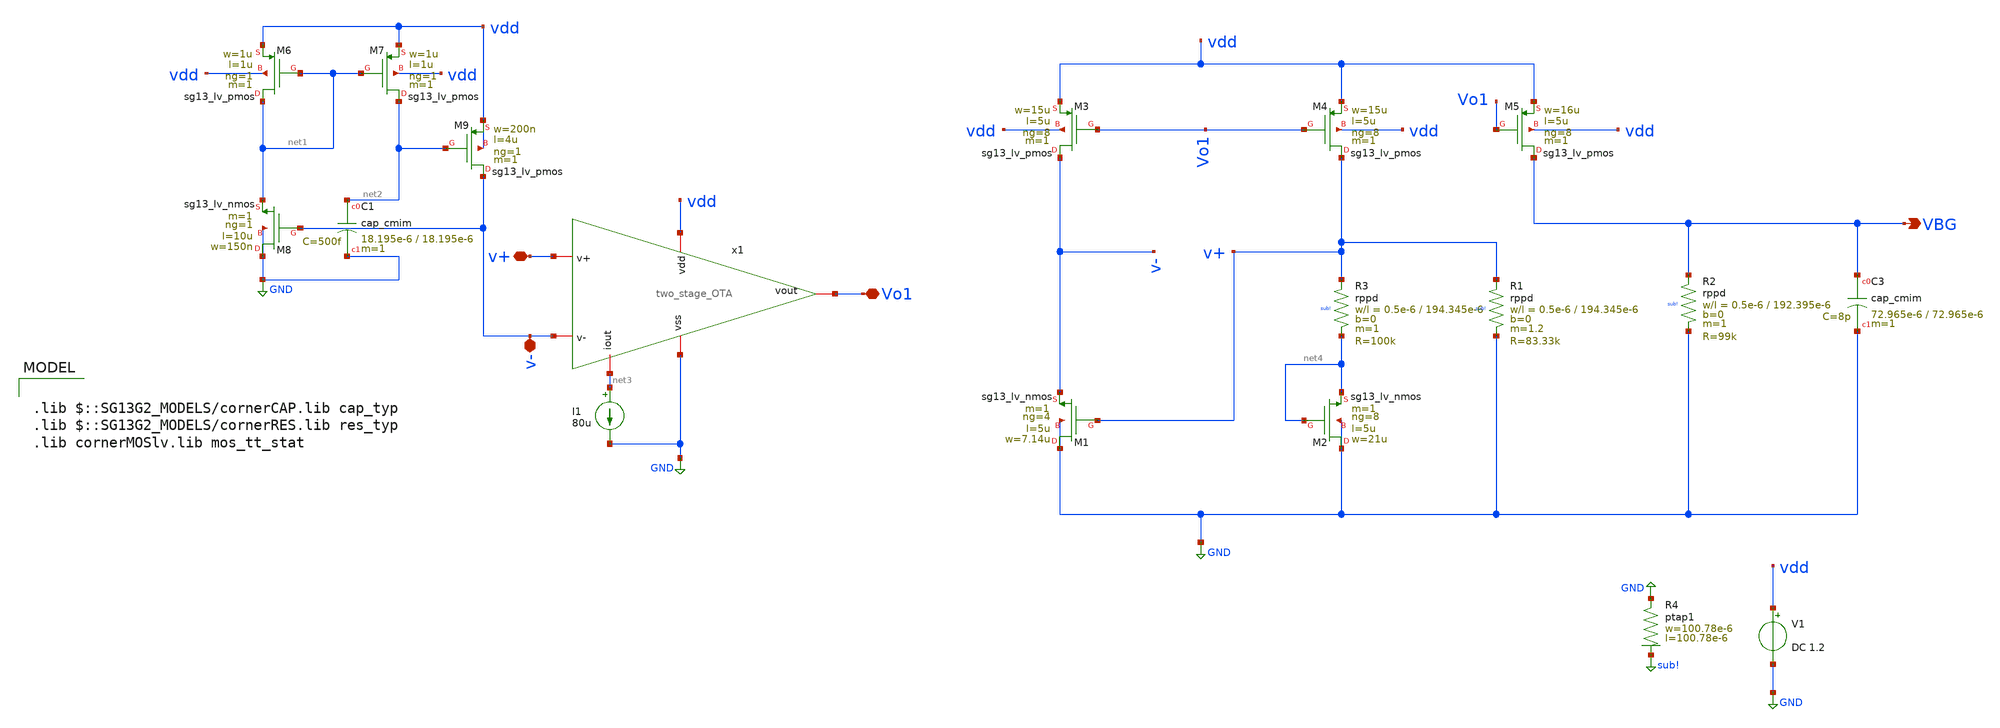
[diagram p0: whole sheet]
** sch_path: modules/module_1_bandgap_reference/part_2_full_bgr/schematic/bandgap_MC.sch
**.subckt bandgap_MC v+ v- Vo1 VBG
*.iopin v+
*.iopin v-
*.iopin Vo1
*.opin VBG
XM8 GND v- net1 GND sg13_lv_nmos w=150n l=10u ng=1 m=1 mm_ok=1
XM6 net1 net1 vdd vdd sg13_lv_pmos w=1u l=1u ng=1 m=1 mm_ok=1
XM7 net2 net1 vdd vdd sg13_lv_pmos w=1u l=1u ng=1 m=1 mm_ok=1
XM9 v- net2 vdd vdd sg13_lv_pmos w=200n l=4u ng=1 m=1 mm_ok=1
I1 net3 GND 80u
V1 vdd GND DC 1.2
XM1 GND v+ v- GND sg13_lv_nmos w=7.14u l=5u ng=4 m=1 mm_ok=1
XM2 GND net4 net4 GND sg13_lv_nmos w=21u l=5u ng=8 m=1 mm_ok=1
XM3 v- Vo1 vdd vdd sg13_lv_pmos w=15u l=5u ng=8 m=1 mm_ok=1
XM4 v+ Vo1 vdd vdd sg13_lv_pmos w=15u l=5u ng=8 m=1 mm_ok=1
XM5 VBG Vo1 vdd vdd sg13_lv_pmos w=16u l=5u ng=8 m=1 mm_ok=1
XC3 VBG GND cap_cmim w=72.965e-6 l=72.965e-6 m=1 mm_ok=1
XR3 v+ net4 sub! rppd w=0.5e-6 l=194.345e-6 m=1 b=0 mm_ok=1
XR1 v+ GND sub! rppd w=0.5e-6 l=194.345e-6 m=1.2 b=0 mm_ok=1
XR2 VBG GND sub! rppd w=0.5e-6 l=192.395e-6 m=1 b=0 mm_ok=1
XC1 net2 GND cap_cmim w=18.195e-6 l=18.195e-6 m=1 mm_ok=1
x1 vdd net3 v+ v- Vo1 GND two_stage_OTA
XR4 GND sub! ptap1 R=92.81m w=100.78e-6 l=100.78e-6
**** begin user architecture code


.param mm_ok=1
.param mc_ok=1

.control
  let run = 1
  let mc_runs = 100
  set curplot = new
  set scratch = $curplot
  dowhile run <= mc_runs
    reset
    dc temp 100 -50 -5
    set run = $&run
    set dc = $curplot
    setplot $scratch
    let off{$run} = {$dc}.v(VBG)
    let mytemp{$run} = "{$dc}.temp-sweep"
    setplot $dc
    let run = run + 1
  end
  set nolegend
  plot {$scratch}.allv vs {$scratch}.mytemp1
  write bandgap_testbench_mc_mis.raw {$scratch}.allv {$scratch}.mytemp1
.endc




.lib $::SG13G2_MODELS/cornerCAP.lib cap_typ
.lib $::SG13G2_MODELS/cornerRES.lib res_typ
.lib cornerMOSlv.lib mos_tt_stat
**** end user architecture code
**.ends

* expanding   symbol:  two_stage_OTA.sym # of pins=6
** sym_path: modules/module_1_bandgap_reference/part_1_OTA/gmid_example/schematic/two_stage_OTA.sym
** sch_path: modules/module_1_bandgap_reference/part_1_OTA/gmid_example/schematic/two_stage_OTA.sch
.subckt two_stage_OTA vdd iout v+ v- vout vss
*.iopin v-
*.iopin v+
*.iopin vss
*.iopin vdd
*.iopin iout
*.iopin vout
XM4 vout net1 vss vss sg13_lv_nmos w=3.09u l=6.24u ng=1 m=1 mm_ok=1
XM3 net1 net1 vss vss sg13_lv_nmos w=3.09u l=6.24u ng=1 m=1 mm_ok=1
XM1 net1 v+ net2 vdd sg13_lv_pmos w=2.75u l=5.46u ng=1 m=1 mm_ok=1
XM5 net2 iout vdd vdd sg13_lv_pmos w=66u l=9.98u ng=10 m=1 mm_ok=1
XM6 iout iout vdd vdd sg13_lv_pmos w=66u l=9.98u ng=10 m=1 mm_ok=1
XM2 vout v- net2 vdd sg13_lv_pmos w=2.75u l=5.46u ng=1 m=1 mm_ok=1
.ends

.GLOBAL GND
.GLOBAL sub!
.end
